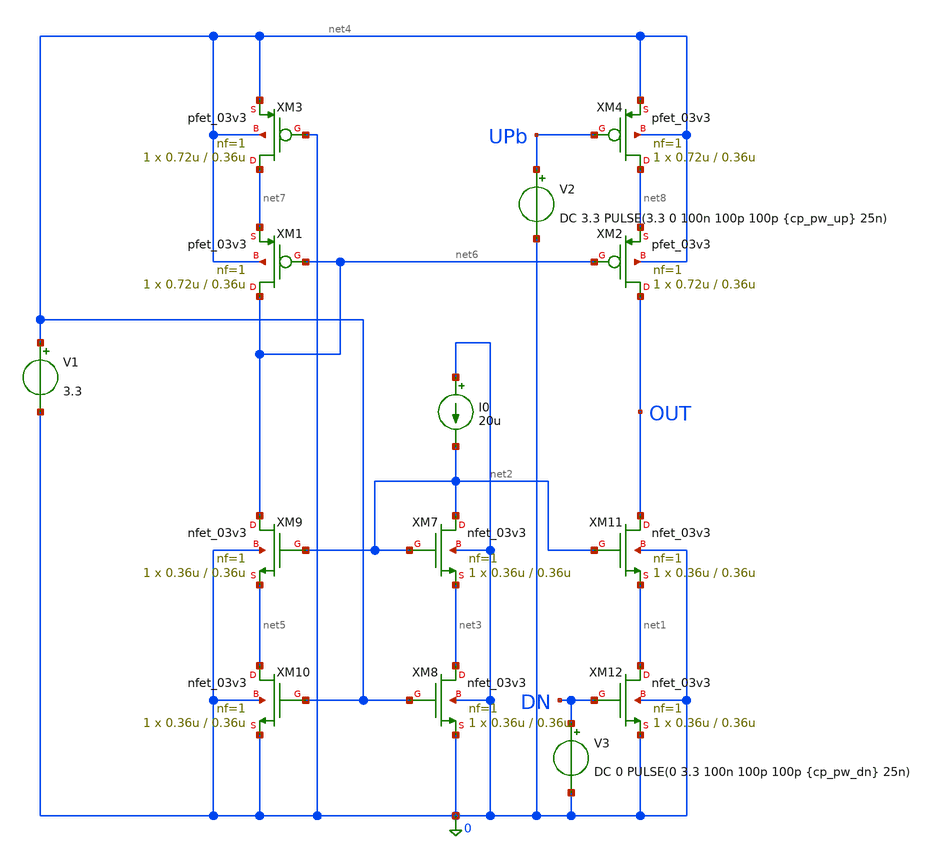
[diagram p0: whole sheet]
** sch_path: PLL/analog/schematics/Charge_Pump_FE.sch
**.subckt Charge_Pump_FE
XM1 net6 net6 net7 net4 pfet_03v3 L=0.36u W=0.72u nf=1 ad='int((nf+1)/2) * W/nf * 0.18u' as='int((nf+2)/2) * W/nf * 0.18u'
+ pd='2*int((nf+1)/2) * (W/nf + 0.18u)' ps='2*int((nf+2)/2) * (W/nf + 0.18u)' nrd='0.18u / W' nrs='0.18u / W'
+ sa=0 sb=0 sd=0 m=1
XM2 OUT net6 net8 net4 pfet_03v3 L=0.36u W=0.72u nf=1 ad='int((nf+1)/2) * W/nf * 0.18u' as='int((nf+2)/2) * W/nf * 0.18u'
+ pd='2*int((nf+1)/2) * (W/nf + 0.18u)' ps='2*int((nf+2)/2) * (W/nf + 0.18u)' nrd='0.18u / W' nrs='0.18u / W'
+ sa=0 sb=0 sd=0 m=1
XM3 net7 0 net4 net4 pfet_03v3 L=0.36u W=0.72u nf=1 ad='int((nf+1)/2) * W/nf * 0.18u' as='int((nf+2)/2) * W/nf * 0.18u'
+ pd='2*int((nf+1)/2) * (W/nf + 0.18u)' ps='2*int((nf+2)/2) * (W/nf + 0.18u)' nrd='0.18u / W' nrs='0.18u / W'
+ sa=0 sb=0 sd=0 m=1
XM4 net8 UPb net4 net4 pfet_03v3 L=0.36u W=0.72u nf=1 ad='int((nf+1)/2) * W/nf * 0.18u' as='int((nf+2)/2) * W/nf * 0.18u'
+ pd='2*int((nf+1)/2) * (W/nf + 0.18u)' ps='2*int((nf+2)/2) * (W/nf + 0.18u)' nrd='0.18u / W' nrs='0.18u / W'
+ sa=0 sb=0 sd=0 m=1
XM7 net2 net2 net3 0 nfet_03v3 L=0.36u W=0.36u nf=1 ad='int((nf+1)/2) * W/nf * 0.18u' as='int((nf+2)/2) * W/nf * 0.18u'
+ pd='2*int((nf+1)/2) * (W/nf + 0.18u)' ps='2*int((nf+2)/2) * (W/nf + 0.18u)' nrd='0.18u / W' nrs='0.18u / W'
+ sa=0 sb=0 sd=0 m=1
XM8 net3 net4 0 0 nfet_03v3 L=0.36u W=0.36u nf=1 ad='int((nf+1)/2) * W/nf * 0.18u' as='int((nf+2)/2) * W/nf * 0.18u'
+ pd='2*int((nf+1)/2) * (W/nf + 0.18u)' ps='2*int((nf+2)/2) * (W/nf + 0.18u)' nrd='0.18u / W' nrs='0.18u / W'
+ sa=0 sb=0 sd=0 m=1
XM9 net6 net2 net5 0 nfet_03v3 L=0.36u W=0.36u nf=1 ad='int((nf+1)/2) * W/nf * 0.18u' as='int((nf+2)/2) * W/nf * 0.18u'
+ pd='2*int((nf+1)/2) * (W/nf + 0.18u)' ps='2*int((nf+2)/2) * (W/nf + 0.18u)' nrd='0.18u / W' nrs='0.18u / W'
+ sa=0 sb=0 sd=0 m=1
XM10 net5 net4 0 0 nfet_03v3 L=0.36u W=0.36u nf=1 ad='int((nf+1)/2) * W/nf * 0.18u' as='int((nf+2)/2) * W/nf * 0.18u'
+ pd='2*int((nf+1)/2) * (W/nf + 0.18u)' ps='2*int((nf+2)/2) * (W/nf + 0.18u)' nrd='0.18u / W' nrs='0.18u / W'
+ sa=0 sb=0 sd=0 m=1
XM11 OUT net2 net1 0 nfet_03v3 L=0.36u W=0.36u nf=1 ad='int((nf+1)/2) * W/nf * 0.18u' as='int((nf+2)/2) * W/nf * 0.18u'
+ pd='2*int((nf+1)/2) * (W/nf + 0.18u)' ps='2*int((nf+2)/2) * (W/nf + 0.18u)' nrd='0.18u / W' nrs='0.18u / W'
+ sa=0 sb=0 sd=0 m=1
XM12 net1 DN 0 0 nfet_03v3 L=0.36u W=0.36u nf=1 ad='int((nf+1)/2) * W/nf * 0.18u' as='int((nf+2)/2) * W/nf * 0.18u'
+ pd='2*int((nf+1)/2) * (W/nf + 0.18u)' ps='2*int((nf+2)/2) * (W/nf + 0.18u)' nrd='0.18u / W' nrs='0.18u / W'
+ sa=0 sb=0 sd=0 m=1
I0 0 net2 20u
V1 net4 0 3.3
V2 UPb 0 DC 3.3 PULSE(3.3 0 100n 100p 100p {cp_pw_up} 25n)
V3 DN 0 DC 0 PULSE(0 3.3 100n 100p 100p {cp_pw_dn} 25n)
**** begin user architecture code



.include /foss/pdks/gf180mcuD/libs.tech/ngspice/design.ngspice
.lib /foss/pdks/gf180mcuD/libs.tech/ngspice/sm141064.ngspice typical
.temp 27

* Pulse plateau widths; 100 ps edges give 12.5 ns
* active time at the 50% voltage crossings.
.param cp_pw_up=12.4n cp_pw_dn=12.4n

* PMOS source switch: active LOW

* NMOS sink switch: active HIGH

* Positive sense current means charge delivered by the pump
VSENSE_TEST OUT cp_load 0

* Test load and output-voltage clamp
CLOAD_TEST cp_load 0 10p
RHOLD_TEST cp_load cp_bias 1m
VBIAS_TEST cp_bias 0 1.65

.ic v(cp_load)=1.65

.control
set noaskquit
set numdgt=7

* ------------------------------------------------------------
* DC output-current sweep
* State 0: both OFF
* State 1: source only
* State 2: sink only
* State 3: both ON
* ------------------------------------------------------------

foreach state 0 1 2 3
  reset
  alter VUP_TEST dc=3.3
  alter VDN_TEST dc=0

  if $state = 1
    alter VUP_TEST dc=0
  end

  if $state = 2
    alter VDN_TEST dc=3.3
  end

  if $state = 3
    alter VUP_TEST dc=0
    alter VDN_TEST dc=3.3
  end

  echo DC_STATE_$state
  dc VBIAS_TEST 0.05 3.25 0.05

  let cp_current = i(VSENSE_TEST)
  meas dc i_mid FIND cp_current AT=1.65

  if $state = 0
    set off_plot=$curplot
  end
  if $state = 1
    set source_plot=$curplot
  end
  if $state = 2
    set sink_plot=$curplot
  end
  if $state = 3
    set both_plot=$curplot
  end
end

plot {$off_plot}.cp_current {$source_plot}.cp_current {$sink_plot}.cp_current {$both_plot}.cp_current
+ title CP_DC_current

* Current and mismatch at approximately OUT = 1.65 V
* source_uA and sink_uA are positive current magnitudes.
let source_uA = 1e6 * {$source_plot}.i_mid
let sink_uA = -1e6 * {$sink_plot}.i_mid
let both_on_uA = 1e6 * {$both_plot}.i_mid
let off_nA = 1e9 * {$off_plot}.i_mid

print source_uA sink_uA both_on_uA off_nA

if (source_uA + sink_uA) gt 1e-6
  let mismatch_pct = 100*(source_uA-sink_uA)/((source_uA+sink_uA)/2)
  print mismatch_pct
end

* ------------------------------------------------------------
* Transient tests with the output clamp effectively disconnected
* Both branches turn ON together, matching the paper's FE-PFD.
*
* Case 1: UP active 12.5 ns, DN active 10.5 ns
* Case 2: UP active 10.5 ns, DN active 12.5 ns
* Case 3: Both active 12.5 ns
* ------------------------------------------------------------

foreach test 1 2 3
  alterparam cp_pw_up=12.4n
  alterparam cp_pw_dn=12.4n

  if $test = 1
    alterparam cp_pw_dn=10.4n
  end

  if $test = 2
    alterparam cp_pw_up=10.4n
  end

  reset

  * Change the clamp resistance from 1 milliohm to 1 teraohm
  alter RHOLD_TEST=1e12

  echo TRANSIENT_CASE_$test
  tran 5p 600n 0 5p

  * Output drift over eight complete clock periods
  meas tran v_start FIND v(OUT) AT=300n
  meas tran v_end FIND v(OUT) AT=500n
  let drift_mV = 1000*(v_end-v_start)

  * Net charge delivered during one complete clock period
  meas tran q_cycle INTEG i(VSENSE_TEST) FROM=400n TO=425n
  let q_cycle_fC = 1e15*q_cycle

  print drift_mV q_cycle_fC

  plot v(OUT) title CP_output_case_{$test}
  plot i(VSENSE_TEST) xlimit 400n 450n title CP_current_case_{$test}
end
.endc



**** end user architecture code
**.ends
.end
